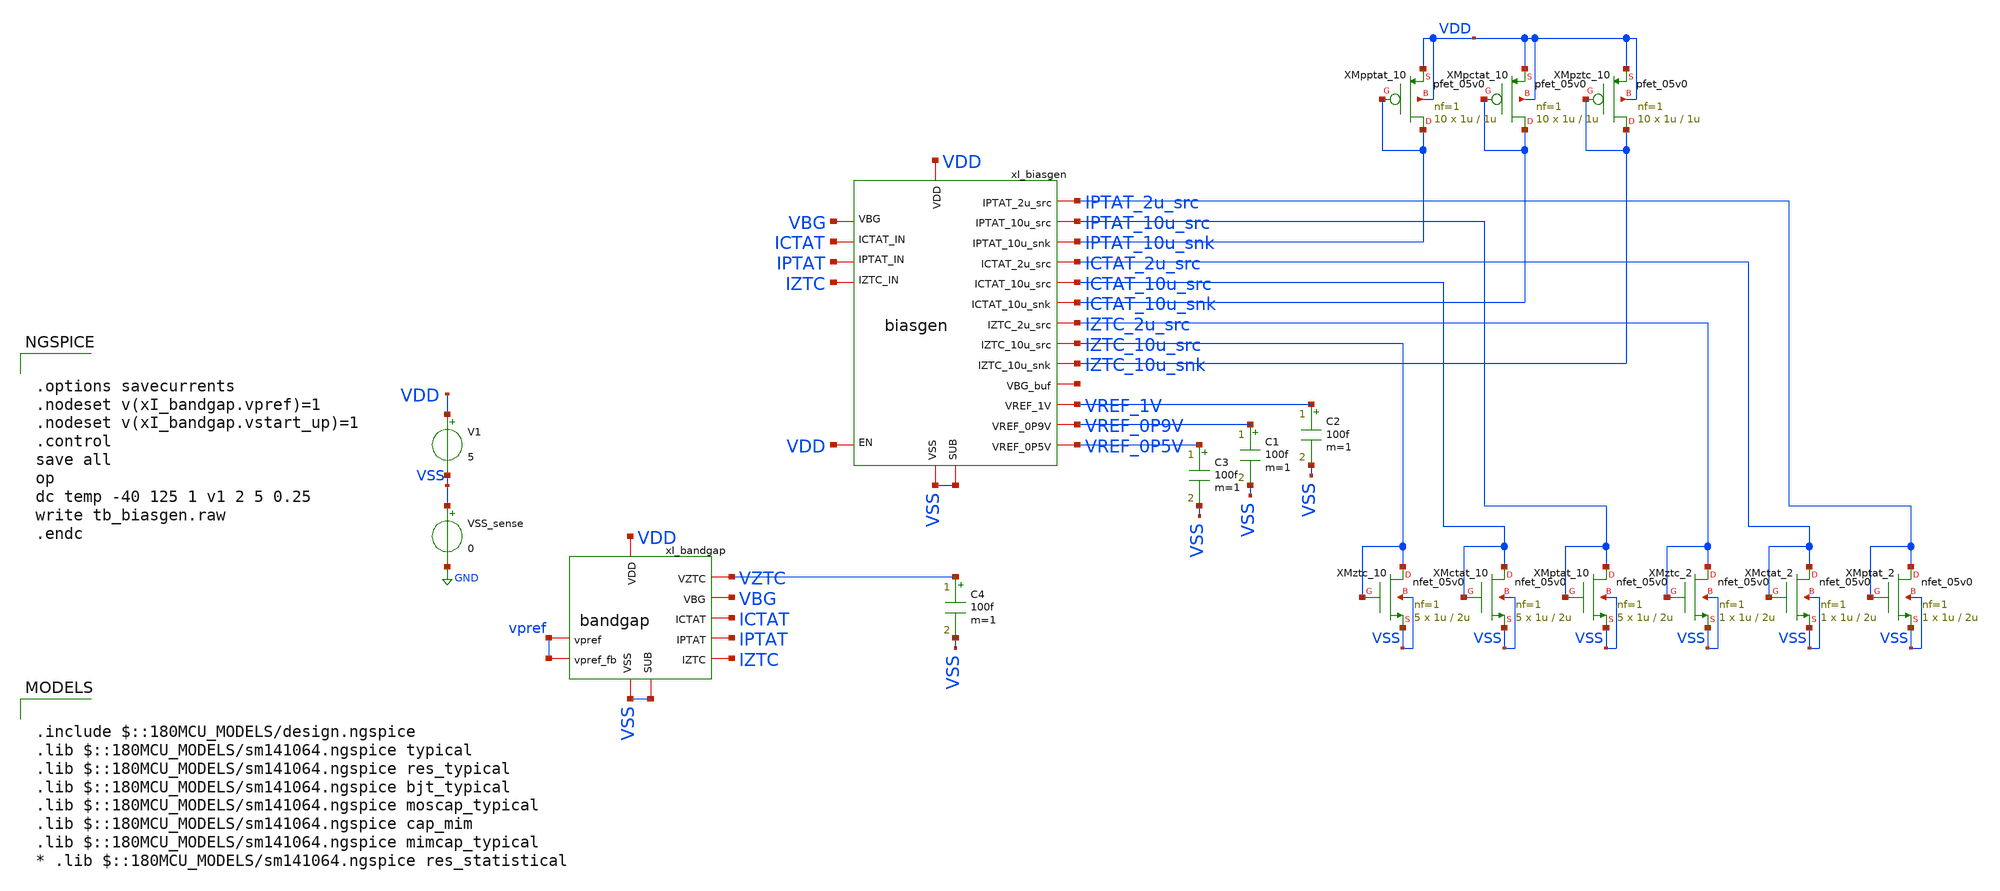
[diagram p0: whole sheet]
** sch_path: designs/libs/tb_biasgen/tb_biasgen/tb_biasgen.sch
**.subckt tb_biasgen
V1 VDD VSS 5
VSS_sense VSS GND 0
C1 VREF_0P9V VSS 100f m=1
xI_bandgap VDD VBG IPTAT IZTC VSS VSS vpref vpref ICTAT VZTC bandgap
C2 VREF_1V VSS 100f m=1
XMztc_2 IZTC_2u_src IZTC_2u_src VSS VSS nfet_05v0 L=2u W=1u nf=1 ad='int((nf+1)/2) * W/nf * 0.18u' as='int((nf+2)/2) * W/nf * 0.18u'
+ pd='2*int((nf+1)/2) * (W/nf + 0.18u)' ps='2*int((nf+2)/2) * (W/nf + 0.18u)' nrd='0.18u / W' nrs='0.18u / W'
+ sa=0 sb=0 sd=0 m=1
XMctat_2 ICTAT_2u_src ICTAT_2u_src VSS VSS nfet_05v0 L=2u W=1u nf=1 ad='int((nf+1)/2) * W/nf * 0.18u'
+ as='int((nf+2)/2) * W/nf * 0.18u' pd='2*int((nf+1)/2) * (W/nf + 0.18u)' ps='2*int((nf+2)/2) * (W/nf + 0.18u)'
+ nrd='0.18u / W' nrs='0.18u / W' sa=0 sb=0 sd=0 m=1
XMptat_2 IPTAT_2u_src IPTAT_2u_src VSS VSS nfet_05v0 L=2u W=1u nf=1 ad='int((nf+1)/2) * W/nf * 0.18u'
+ as='int((nf+2)/2) * W/nf * 0.18u' pd='2*int((nf+1)/2) * (W/nf + 0.18u)' ps='2*int((nf+2)/2) * (W/nf + 0.18u)'
+ nrd='0.18u / W' nrs='0.18u / W' sa=0 sb=0 sd=0 m=1
xI_biasgen VDD VBG IPTAT_2u_src IPTAT VREF_1V IZTC VREF_0P5V VSS VSS VREF_0P9V ICTAT IPTAT_10u_src
+ IPTAT_10u_snk ICTAT_2u_src ICTAT_10u_src ICTAT_10u_snk IZTC_2u_src IZTC_10u_src IZTC_10u_snk VDD net1 biasgen
C3 VREF_0P5V VSS 100f m=1
XMztc_10 IZTC_10u_src IZTC_10u_src VSS VSS nfet_05v0 L=2u W=1u nf=1 ad='int((nf+1)/2) * W/nf * 0.18u'
+ as='int((nf+2)/2) * W/nf * 0.18u' pd='2*int((nf+1)/2) * (W/nf + 0.18u)' ps='2*int((nf+2)/2) * (W/nf + 0.18u)'
+ nrd='0.18u / W' nrs='0.18u / W' sa=0 sb=0 sd=0 m=5
XMctat_10 ICTAT_10u_src ICTAT_10u_src VSS VSS nfet_05v0 L=2u W=1u nf=1 ad='int((nf+1)/2) * W/nf * 0.18u'
+ as='int((nf+2)/2) * W/nf * 0.18u' pd='2*int((nf+1)/2) * (W/nf + 0.18u)' ps='2*int((nf+2)/2) * (W/nf + 0.18u)'
+ nrd='0.18u / W' nrs='0.18u / W' sa=0 sb=0 sd=0 m=5
XMptat_10 IPTAT_10u_src IPTAT_10u_src VSS VSS nfet_05v0 L=2u W=1u nf=1 ad='int((nf+1)/2) * W/nf * 0.18u'
+ as='int((nf+2)/2) * W/nf * 0.18u' pd='2*int((nf+1)/2) * (W/nf + 0.18u)' ps='2*int((nf+2)/2) * (W/nf + 0.18u)'
+ nrd='0.18u / W' nrs='0.18u / W' sa=0 sb=0 sd=0 m=5
XMpptat_10 IPTAT_10u_snk IPTAT_10u_snk VDD VDD pfet_05v0 L=1u W=1u nf=1 ad='int((nf+1)/2) * W/nf * 0.18u'
+ as='int((nf+2)/2) * W/nf * 0.18u' pd='2*int((nf+1)/2) * (W/nf + 0.18u)' ps='2*int((nf+2)/2) * (W/nf + 0.18u)'
+ nrd='0.18u / W' nrs='0.18u / W' sa=0 sb=0 sd=0 m=10
XMpctat_10 ICTAT_10u_snk ICTAT_10u_snk VDD VDD pfet_05v0 L=1u W=1u nf=1 ad='int((nf+1)/2) * W/nf * 0.18u'
+ as='int((nf+2)/2) * W/nf * 0.18u' pd='2*int((nf+1)/2) * (W/nf + 0.18u)' ps='2*int((nf+2)/2) * (W/nf + 0.18u)'
+ nrd='0.18u / W' nrs='0.18u / W' sa=0 sb=0 sd=0 m=10
XMpztc_10 IZTC_10u_snk IZTC_10u_snk VDD VDD pfet_05v0 L=1u W=1u nf=1 ad='int((nf+1)/2) * W/nf * 0.18u'
+ as='int((nf+2)/2) * W/nf * 0.18u' pd='2*int((nf+1)/2) * (W/nf + 0.18u)' ps='2*int((nf+2)/2) * (W/nf + 0.18u)'
+ nrd='0.18u / W' nrs='0.18u / W' sa=0 sb=0 sd=0 m=10
C4 VZTC VSS 100f m=1
**** begin user architecture code

.include $::180MCU_MODELS/design.ngspice
.lib $::180MCU_MODELS/sm141064.ngspice typical
.lib $::180MCU_MODELS/sm141064.ngspice res_typical
.lib $::180MCU_MODELS/sm141064.ngspice bjt_typical
.lib $::180MCU_MODELS/sm141064.ngspice moscap_typical
.lib $::180MCU_MODELS/sm141064.ngspice cap_mim
.lib $::180MCU_MODELS/sm141064.ngspice mimcap_typical
* .lib $::180MCU_MODELS/sm141064.ngspice res_statistical



.options savecurrents
.nodeset v(xI_bandgap.vpref)=1
.nodeset v(xI_bandgap.vstart_up)=1
.control
save all
op
dc temp -40 125 1 v1 2 5 0.25
write tb_biasgen.raw
.endc


**** end user architecture code
**.ends
.GLOBAL GND
.end
